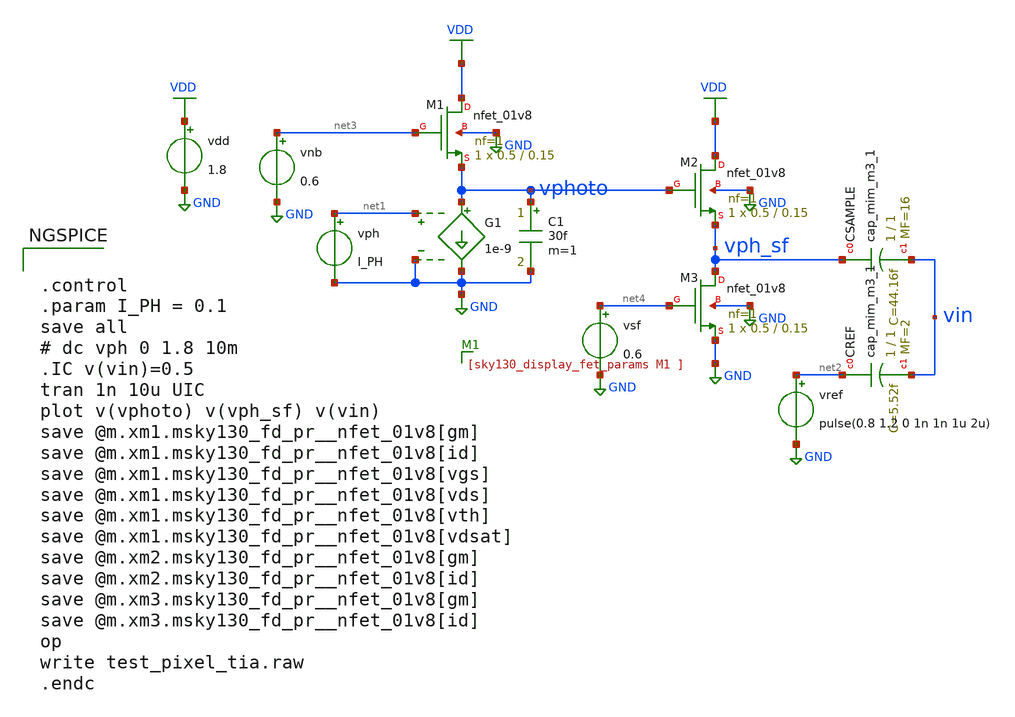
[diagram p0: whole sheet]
** sch_path: analog/klayout/production/final_merge_20260923/testbenches/cace/analog/xschem/test_pixel_tia.sch
**.subckt test_pixel_tia
vdd VDD GND 1.8
.save i(vdd)
XCSAMPLE vph_sf vin sky130_fd_pr__cap_mim_m3_1 W=1 L=1 MF=16 m=16
XCREF net2 vin sky130_fd_pr__cap_mim_m3_1 W=1 L=1 MF=2 m=2
C1 vphoto GND 30f m=1
vph net1 GND I_PH
XM1 VDD net3 vphoto GND sky130_fd_pr__nfet_01v8 L=0.15 W=0.5 nf=1 ad='int((1 + 1)/2) * 0.5 / 1 * 0.29'
+ as='int((1 + 2)/2) * 0.5 / 1 * 0.29' pd='2*int((1 + 1)/2) * (0.5 / 1 + 0.29)' ps='2*int((1 + 2)/2) * (0.5 / 1 + 0.29)'
+ nrd='0.29 / 0.5 ' nrs='0.29 / 0.5 ' sa=0 sb=0 sd=0 mult=1 m=1
G1 vphoto GND net1 GND 1e-9
vnb net3 GND 0.6
XM2 VDD vphoto vph_sf GND sky130_fd_pr__nfet_01v8 L=0.15 W=0.5 nf=1 ad='int((1 + 1)/2) * 0.5 / 1 * 0.29'
+ as='int((1 + 2)/2) * 0.5 / 1 * 0.29' pd='2*int((1 + 1)/2) * (0.5 / 1 + 0.29)' ps='2*int((1 + 2)/2) * (0.5 / 1 + 0.29)'
+ nrd='0.29 / 0.5 ' nrs='0.29 / 0.5 ' sa=0 sb=0 sd=0 mult=1 m=1
XM3 vph_sf net4 GND GND sky130_fd_pr__nfet_01v8 L=0.15 W=0.5 nf=1 ad='int((1 + 1)/2) * 0.5 / 1 * 0.29'
+ as='int((1 + 2)/2) * 0.5 / 1 * 0.29' pd='2*int((1 + 1)/2) * (0.5 / 1 + 0.29)' ps='2*int((1 + 2)/2) * (0.5 / 1 + 0.29)'
+ nrd='0.29 / 0.5 ' nrs='0.29 / 0.5 ' sa=0 sb=0 sd=0 mult=1 m=1
vsf net4 GND 0.6
vref net2 GND pulse(0.8 1.2 0 1n 1n 1u 2u)
**** begin user architecture code

** opencircuitdesign pdks install
.lib $::SKYWATER_MODELS/sky130.lib.spice tt



.control
.param I_PH = 0.1
save all
# dc vph 0 1.8 10m
.IC v(vin)=0.5
tran 1n 10u UIC
plot v(vphoto) v(vph_sf) v(vin)
save @m.xm1.msky130_fd_pr__nfet_01v8[gm]
save @m.xm1.msky130_fd_pr__nfet_01v8[id]
save @m.xm1.msky130_fd_pr__nfet_01v8[vgs]
save @m.xm1.msky130_fd_pr__nfet_01v8[vds]
save @m.xm1.msky130_fd_pr__nfet_01v8[vth]
save @m.xm1.msky130_fd_pr__nfet_01v8[vdsat]
save @m.xm2.msky130_fd_pr__nfet_01v8[gm]
save @m.xm2.msky130_fd_pr__nfet_01v8[id]
save @m.xm3.msky130_fd_pr__nfet_01v8[gm]
save @m.xm3.msky130_fd_pr__nfet_01v8[id]
op
write test_pixel_tia.raw
.endc


**** end user architecture code
**.ends
.GLOBAL VDD
.GLOBAL GND
.end
